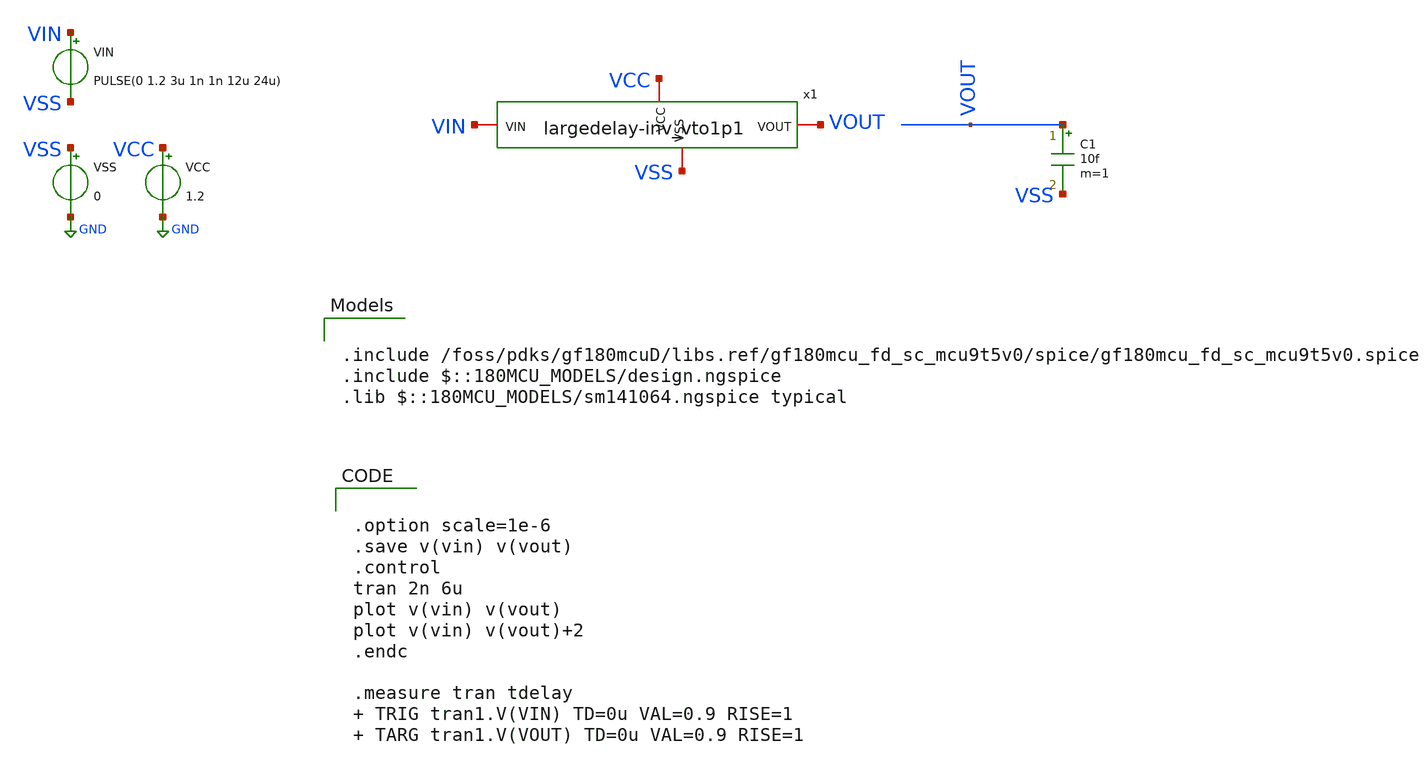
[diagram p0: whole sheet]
** sch_path: xschem/large_delay/tb_largedelay-inv_vto1p1.sch
**.subckt tb_largedelay-inv_vto1p1
VCC VCC GND 1.2
VSS VSS GND 0
VIN VIN VSS PULSE(0 1.2 3u 1n 1n 12u 24u)
C1 VOUT VSS 10f m=1
x1 VCC VSS VIN VOUT largedelay-inv_vto1p1
**** begin user architecture code


.option scale=1e-6
.save v(vin) v(vout)
.control
tran 2n 6u
plot v(vin) v(vout)
plot v(vin) v(vout)+2
.endc

.measure tran tdelay  TRIG tran1.V(VIN) TD=0u VAL=0.9 RISE=1  TARG tran1.V(VOUT) TD=0u VAL=0.9
+ RISE=1





.include /foss/pdks/gf180mcuD/libs.ref/gf180mcu_fd_sc_mcu9t5v0/spice/gf180mcu_fd_sc_mcu9t5v0.spice
.include $::180MCU_MODELS/design.ngspice
.lib $::180MCU_MODELS/sm141064.ngspice typical

**** end user architecture code
**.ends

* expanding   symbol:  largedelay-inv_vto1p1.sym # of pins=4
** sym_path: xschem/large_delay/largedelay-inv_vto1p1.sym
** sch_path: xschem/large_delay/largedelay-inv_vto1p1.sch
.subckt largedelay-inv_vto1p1 VCC VSS VIN VOUT
*.iopin VIN
*.iopin VOUT
*.iopin VCC
*.iopin VSS
x1[0] VIN VSS VCC VSS VCC n2 gf180mcu_fd_sc_mcu9t5v0__inv_1
x1[1] n2 VSS VCC VSS VCC n3 gf180mcu_fd_sc_mcu9t5v0__inv_1
x1[2] n3 VSS VCC VSS VCC n4 gf180mcu_fd_sc_mcu9t5v0__inv_1
x1[3] n4 VSS VCC VSS VCC n5 gf180mcu_fd_sc_mcu9t5v0__inv_1
x1[4] n5 VSS VCC VSS VCC n6 gf180mcu_fd_sc_mcu9t5v0__inv_1
x1[5] n6 VSS VCC VSS VCC VOUT gf180mcu_fd_sc_mcu9t5v0__inv_1
.ends

.GLOBAL GND
.end
